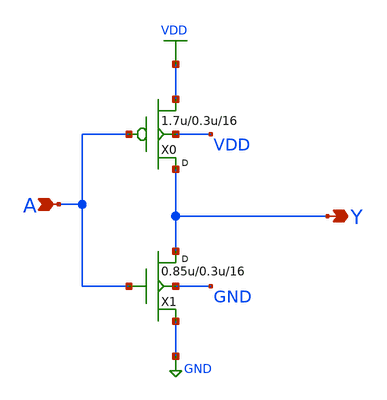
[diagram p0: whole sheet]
** sch_path: gf180mcu_osu_sc_gp12t3v3/cells/inv/gf180mcu_osu_sc_gp12t3v3__inv_16.sch
**.subckt gf180mcu_osu_sc_gp12t3v3__inv_16 A Y
*.ipin A
*.opin Y
X0 Y A VDD VDD pfet_03p3 w=1.7u l=0.3u m=16
X1 Y A GND GND nfet_03p3 w=0.85u l=0.3u m=16
**.ends
.GLOBAL VDD
.GLOBAL GND
.end
